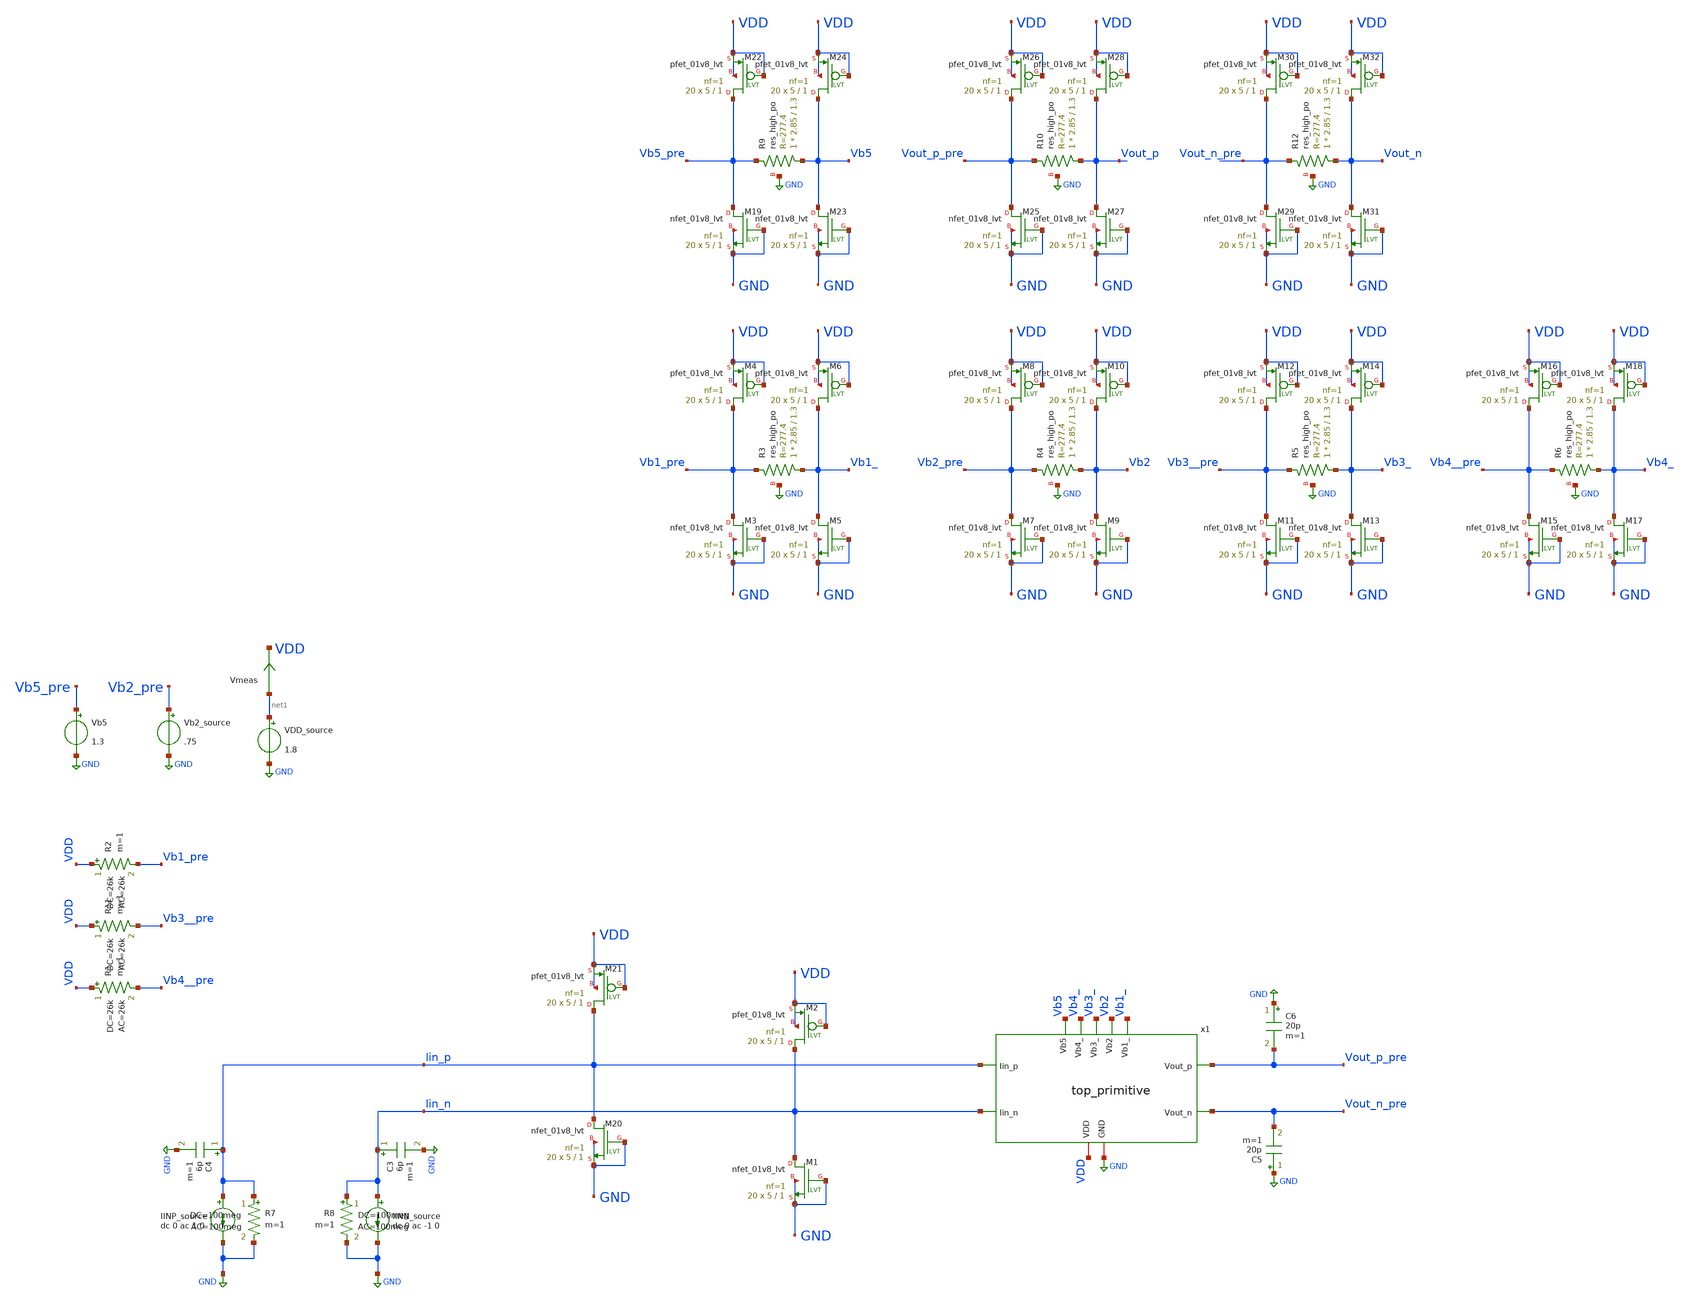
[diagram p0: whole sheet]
** sch_path: xschem/top_pex_tb.sch
**.subckt top_pex_tb
VDD_source net1 GND 1.8
Vmeas net1 VDD 0
.save i(vmeas)
Vb2_source Vb2_pre GND .75
C3 Iin_n GND 6p m=1
C4 Iin_p GND 6p m=1
IINP_source Iin_p GND dc 0 ac 1 0
IINN_source Iin_n GND dc 0 ac -1 0
C5 GND Vout_n_pre 20p m=1
C6 GND Vout_p_pre 20p m=1
R7 Iin_p GND 100meg ac=100meg m=1
R8 Iin_n GND 100meg ac=100meg m=1
Vb5 Vb5_pre GND 1.3
R2 VDD Vb1_pre 26k ac=26k m=1
R11 VDD Vb3__pre 26k ac=26k m=1
x1 Iin_p Iin_n Vb1_ Vb2 Vb3_ Vb4_ Vb5 VDD GND Vout_n_pre Vout_p_pre top_primitive
R1 VDD Vb4__pre 26k ac=26k m=1
XM20 Iin_p GND GND GND sky130_fd_pr__nfet_01v8_lvt L=1 W=5 nf=1 ad='int((nf+1)/2) * W/nf * 0.29' as='int((nf+2)/2) * W/nf * 0.29'
+ pd='2*int((nf+1)/2) * (W/nf + 0.29)' ps='2*int((nf+2)/2) * (W/nf + 0.29)' nrd='0.29 / W' nrs='0.29 / W'
+ sa=0 sb=0 sd=0 mult=20 m=20
XM21 Iin_p VDD VDD VDD sky130_fd_pr__pfet_01v8_lvt L=1 W=5 nf=1 ad='int((nf+1)/2) * W/nf * 0.29' as='int((nf+2)/2) * W/nf * 0.29'
+ pd='2*int((nf+1)/2) * (W/nf + 0.29)' ps='2*int((nf+2)/2) * (W/nf + 0.29)' nrd='0.29 / W' nrs='0.29 / W'
+ sa=0 sb=0 sd=0 mult=20 m=20
XM1 Iin_n GND GND GND sky130_fd_pr__nfet_01v8_lvt L=1 W=5 nf=1 ad='int((nf+1)/2) * W/nf * 0.29' as='int((nf+2)/2) * W/nf * 0.29'
+ pd='2*int((nf+1)/2) * (W/nf + 0.29)' ps='2*int((nf+2)/2) * (W/nf + 0.29)' nrd='0.29 / W' nrs='0.29 / W'
+ sa=0 sb=0 sd=0 mult=20 m=20
XM2 Iin_n VDD VDD VDD sky130_fd_pr__pfet_01v8_lvt L=1 W=5 nf=1 ad='int((nf+1)/2) * W/nf * 0.29' as='int((nf+2)/2) * W/nf * 0.29'
+ pd='2*int((nf+1)/2) * (W/nf + 0.29)' ps='2*int((nf+2)/2) * (W/nf + 0.29)' nrd='0.29 / W' nrs='0.29 / W'
+ sa=0 sb=0 sd=0 mult=20 m=20
XM3 Vb1_pre GND GND GND sky130_fd_pr__nfet_01v8_lvt L=1 W=5 nf=1 ad='int((nf+1)/2) * W/nf * 0.29' as='int((nf+2)/2) * W/nf * 0.29'
+ pd='2*int((nf+1)/2) * (W/nf + 0.29)' ps='2*int((nf+2)/2) * (W/nf + 0.29)' nrd='0.29 / W' nrs='0.29 / W'
+ sa=0 sb=0 sd=0 mult=20 m=20
XM4 Vb1_pre VDD VDD VDD sky130_fd_pr__pfet_01v8_lvt L=1 W=5 nf=1 ad='int((nf+1)/2) * W/nf * 0.29' as='int((nf+2)/2) * W/nf * 0.29'
+ pd='2*int((nf+1)/2) * (W/nf + 0.29)' ps='2*int((nf+2)/2) * (W/nf + 0.29)' nrd='0.29 / W' nrs='0.29 / W'
+ sa=0 sb=0 sd=0 mult=20 m=20
XM5 Vb1_ GND GND GND sky130_fd_pr__nfet_01v8_lvt L=1 W=5 nf=1 ad='int((nf+1)/2) * W/nf * 0.29' as='int((nf+2)/2) * W/nf * 0.29'
+ pd='2*int((nf+1)/2) * (W/nf + 0.29)' ps='2*int((nf+2)/2) * (W/nf + 0.29)' nrd='0.29 / W' nrs='0.29 / W'
+ sa=0 sb=0 sd=0 mult=20 m=20
XM6 Vb1_ VDD VDD VDD sky130_fd_pr__pfet_01v8_lvt L=1 W=5 nf=1 ad='int((nf+1)/2) * W/nf * 0.29' as='int((nf+2)/2) * W/nf * 0.29'
+ pd='2*int((nf+1)/2) * (W/nf + 0.29)' ps='2*int((nf+2)/2) * (W/nf + 0.29)' nrd='0.29 / W' nrs='0.29 / W'
+ sa=0 sb=0 sd=0 mult=20 m=20
XR3 Vb1_ Vb1_pre GND sky130_fd_pr__res_high_po W=2.85 L=1.3 mult=1 m=1
XM7 Vb2_pre GND GND GND sky130_fd_pr__nfet_01v8_lvt L=1 W=5 nf=1 ad='int((nf+1)/2) * W/nf * 0.29' as='int((nf+2)/2) * W/nf * 0.29'
+ pd='2*int((nf+1)/2) * (W/nf + 0.29)' ps='2*int((nf+2)/2) * (W/nf + 0.29)' nrd='0.29 / W' nrs='0.29 / W'
+ sa=0 sb=0 sd=0 mult=20 m=20
XM8 Vb2_pre VDD VDD VDD sky130_fd_pr__pfet_01v8_lvt L=1 W=5 nf=1 ad='int((nf+1)/2) * W/nf * 0.29' as='int((nf+2)/2) * W/nf * 0.29'
+ pd='2*int((nf+1)/2) * (W/nf + 0.29)' ps='2*int((nf+2)/2) * (W/nf + 0.29)' nrd='0.29 / W' nrs='0.29 / W'
+ sa=0 sb=0 sd=0 mult=20 m=20
XM9 Vb2 GND GND GND sky130_fd_pr__nfet_01v8_lvt L=1 W=5 nf=1 ad='int((nf+1)/2) * W/nf * 0.29' as='int((nf+2)/2) * W/nf * 0.29'
+ pd='2*int((nf+1)/2) * (W/nf + 0.29)' ps='2*int((nf+2)/2) * (W/nf + 0.29)' nrd='0.29 / W' nrs='0.29 / W'
+ sa=0 sb=0 sd=0 mult=20 m=20
XM10 Vb2 VDD VDD VDD sky130_fd_pr__pfet_01v8_lvt L=1 W=5 nf=1 ad='int((nf+1)/2) * W/nf * 0.29' as='int((nf+2)/2) * W/nf * 0.29'
+ pd='2*int((nf+1)/2) * (W/nf + 0.29)' ps='2*int((nf+2)/2) * (W/nf + 0.29)' nrd='0.29 / W' nrs='0.29 / W'
+ sa=0 sb=0 sd=0 mult=20 m=20
XR4 Vb2 Vb2_pre GND sky130_fd_pr__res_high_po W=2.85 L=1.3 mult=1 m=1
XM11 Vb3__pre GND GND GND sky130_fd_pr__nfet_01v8_lvt L=1 W=5 nf=1 ad='int((nf+1)/2) * W/nf * 0.29' as='int((nf+2)/2) * W/nf * 0.29'
+ pd='2*int((nf+1)/2) * (W/nf + 0.29)' ps='2*int((nf+2)/2) * (W/nf + 0.29)' nrd='0.29 / W' nrs='0.29 / W'
+ sa=0 sb=0 sd=0 mult=20 m=20
XM12 Vb3__pre VDD VDD VDD sky130_fd_pr__pfet_01v8_lvt L=1 W=5 nf=1 ad='int((nf+1)/2) * W/nf * 0.29' as='int((nf+2)/2) * W/nf * 0.29'
+ pd='2*int((nf+1)/2) * (W/nf + 0.29)' ps='2*int((nf+2)/2) * (W/nf + 0.29)' nrd='0.29 / W' nrs='0.29 / W'
+ sa=0 sb=0 sd=0 mult=20 m=20
XM13 Vb3_ GND GND GND sky130_fd_pr__nfet_01v8_lvt L=1 W=5 nf=1 ad='int((nf+1)/2) * W/nf * 0.29' as='int((nf+2)/2) * W/nf * 0.29'
+ pd='2*int((nf+1)/2) * (W/nf + 0.29)' ps='2*int((nf+2)/2) * (W/nf + 0.29)' nrd='0.29 / W' nrs='0.29 / W'
+ sa=0 sb=0 sd=0 mult=20 m=20
XM14 Vb3_ VDD VDD VDD sky130_fd_pr__pfet_01v8_lvt L=1 W=5 nf=1 ad='int((nf+1)/2) * W/nf * 0.29' as='int((nf+2)/2) * W/nf * 0.29'
+ pd='2*int((nf+1)/2) * (W/nf + 0.29)' ps='2*int((nf+2)/2) * (W/nf + 0.29)' nrd='0.29 / W' nrs='0.29 / W'
+ sa=0 sb=0 sd=0 mult=20 m=20
XR5 Vb3_ Vb3__pre GND sky130_fd_pr__res_high_po W=2.85 L=1.3 mult=1 m=1
XM15 Vb4__pre GND GND GND sky130_fd_pr__nfet_01v8_lvt L=1 W=5 nf=1 ad='int((nf+1)/2) * W/nf * 0.29' as='int((nf+2)/2) * W/nf * 0.29'
+ pd='2*int((nf+1)/2) * (W/nf + 0.29)' ps='2*int((nf+2)/2) * (W/nf + 0.29)' nrd='0.29 / W' nrs='0.29 / W'
+ sa=0 sb=0 sd=0 mult=20 m=20
XM16 Vb4__pre VDD VDD VDD sky130_fd_pr__pfet_01v8_lvt L=1 W=5 nf=1 ad='int((nf+1)/2) * W/nf * 0.29' as='int((nf+2)/2) * W/nf * 0.29'
+ pd='2*int((nf+1)/2) * (W/nf + 0.29)' ps='2*int((nf+2)/2) * (W/nf + 0.29)' nrd='0.29 / W' nrs='0.29 / W'
+ sa=0 sb=0 sd=0 mult=20 m=20
XM17 Vb4_ GND GND GND sky130_fd_pr__nfet_01v8_lvt L=1 W=5 nf=1 ad='int((nf+1)/2) * W/nf * 0.29' as='int((nf+2)/2) * W/nf * 0.29'
+ pd='2*int((nf+1)/2) * (W/nf + 0.29)' ps='2*int((nf+2)/2) * (W/nf + 0.29)' nrd='0.29 / W' nrs='0.29 / W'
+ sa=0 sb=0 sd=0 mult=20 m=20
XM18 Vb4_ VDD VDD VDD sky130_fd_pr__pfet_01v8_lvt L=1 W=5 nf=1 ad='int((nf+1)/2) * W/nf * 0.29' as='int((nf+2)/2) * W/nf * 0.29'
+ pd='2*int((nf+1)/2) * (W/nf + 0.29)' ps='2*int((nf+2)/2) * (W/nf + 0.29)' nrd='0.29 / W' nrs='0.29 / W'
+ sa=0 sb=0 sd=0 mult=20 m=20
XR6 Vb4_ Vb4__pre GND sky130_fd_pr__res_high_po W=2.85 L=1.3 mult=1 m=1
XM19 Vb5_pre GND GND GND sky130_fd_pr__nfet_01v8_lvt L=1 W=5 nf=1 ad='int((nf+1)/2) * W/nf * 0.29' as='int((nf+2)/2) * W/nf * 0.29'
+ pd='2*int((nf+1)/2) * (W/nf + 0.29)' ps='2*int((nf+2)/2) * (W/nf + 0.29)' nrd='0.29 / W' nrs='0.29 / W'
+ sa=0 sb=0 sd=0 mult=20 m=20
XM22 Vb5_pre VDD VDD VDD sky130_fd_pr__pfet_01v8_lvt L=1 W=5 nf=1 ad='int((nf+1)/2) * W/nf * 0.29' as='int((nf+2)/2) * W/nf * 0.29'
+ pd='2*int((nf+1)/2) * (W/nf + 0.29)' ps='2*int((nf+2)/2) * (W/nf + 0.29)' nrd='0.29 / W' nrs='0.29 / W'
+ sa=0 sb=0 sd=0 mult=20 m=20
XM23 Vb5 GND GND GND sky130_fd_pr__nfet_01v8_lvt L=1 W=5 nf=1 ad='int((nf+1)/2) * W/nf * 0.29' as='int((nf+2)/2) * W/nf * 0.29'
+ pd='2*int((nf+1)/2) * (W/nf + 0.29)' ps='2*int((nf+2)/2) * (W/nf + 0.29)' nrd='0.29 / W' nrs='0.29 / W'
+ sa=0 sb=0 sd=0 mult=20 m=20
XM24 Vb5 VDD VDD VDD sky130_fd_pr__pfet_01v8_lvt L=1 W=5 nf=1 ad='int((nf+1)/2) * W/nf * 0.29' as='int((nf+2)/2) * W/nf * 0.29'
+ pd='2*int((nf+1)/2) * (W/nf + 0.29)' ps='2*int((nf+2)/2) * (W/nf + 0.29)' nrd='0.29 / W' nrs='0.29 / W'
+ sa=0 sb=0 sd=0 mult=20 m=20
XR9 Vb5 Vb5_pre GND sky130_fd_pr__res_high_po W=2.85 L=1.3 mult=1 m=1
XM25 Vout_p_pre GND GND GND sky130_fd_pr__nfet_01v8_lvt L=1 W=5 nf=1 ad='int((nf+1)/2) * W/nf * 0.29'
+ as='int((nf+2)/2) * W/nf * 0.29' pd='2*int((nf+1)/2) * (W/nf + 0.29)' ps='2*int((nf+2)/2) * (W/nf + 0.29)'
+ nrd='0.29 / W' nrs='0.29 / W' sa=0 sb=0 sd=0 mult=20 m=20
XM26 Vout_p_pre VDD VDD VDD sky130_fd_pr__pfet_01v8_lvt L=1 W=5 nf=1 ad='int((nf+1)/2) * W/nf * 0.29'
+ as='int((nf+2)/2) * W/nf * 0.29' pd='2*int((nf+1)/2) * (W/nf + 0.29)' ps='2*int((nf+2)/2) * (W/nf + 0.29)'
+ nrd='0.29 / W' nrs='0.29 / W' sa=0 sb=0 sd=0 mult=20 m=20
XM27 Vout_p GND GND GND sky130_fd_pr__nfet_01v8_lvt L=1 W=5 nf=1 ad='int((nf+1)/2) * W/nf * 0.29' as='int((nf+2)/2) * W/nf * 0.29'
+ pd='2*int((nf+1)/2) * (W/nf + 0.29)' ps='2*int((nf+2)/2) * (W/nf + 0.29)' nrd='0.29 / W' nrs='0.29 / W'
+ sa=0 sb=0 sd=0 mult=20 m=20
XM28 Vout_p VDD VDD VDD sky130_fd_pr__pfet_01v8_lvt L=1 W=5 nf=1 ad='int((nf+1)/2) * W/nf * 0.29' as='int((nf+2)/2) * W/nf * 0.29'
+ pd='2*int((nf+1)/2) * (W/nf + 0.29)' ps='2*int((nf+2)/2) * (W/nf + 0.29)' nrd='0.29 / W' nrs='0.29 / W'
+ sa=0 sb=0 sd=0 mult=20 m=20
XR10 Vout_p Vout_p_pre GND sky130_fd_pr__res_high_po W=2.85 L=1.3 mult=1 m=1
XM29 Vout_n_pre GND GND GND sky130_fd_pr__nfet_01v8_lvt L=1 W=5 nf=1 ad='int((nf+1)/2) * W/nf * 0.29'
+ as='int((nf+2)/2) * W/nf * 0.29' pd='2*int((nf+1)/2) * (W/nf + 0.29)' ps='2*int((nf+2)/2) * (W/nf + 0.29)'
+ nrd='0.29 / W' nrs='0.29 / W' sa=0 sb=0 sd=0 mult=20 m=20
XM30 Vout_n_pre VDD VDD VDD sky130_fd_pr__pfet_01v8_lvt L=1 W=5 nf=1 ad='int((nf+1)/2) * W/nf * 0.29'
+ as='int((nf+2)/2) * W/nf * 0.29' pd='2*int((nf+1)/2) * (W/nf + 0.29)' ps='2*int((nf+2)/2) * (W/nf + 0.29)'
+ nrd='0.29 / W' nrs='0.29 / W' sa=0 sb=0 sd=0 mult=20 m=20
XM31 Vout_n GND GND GND sky130_fd_pr__nfet_01v8_lvt L=1 W=5 nf=1 ad='int((nf+1)/2) * W/nf * 0.29' as='int((nf+2)/2) * W/nf * 0.29'
+ pd='2*int((nf+1)/2) * (W/nf + 0.29)' ps='2*int((nf+2)/2) * (W/nf + 0.29)' nrd='0.29 / W' nrs='0.29 / W'
+ sa=0 sb=0 sd=0 mult=20 m=20
XM32 Vout_n VDD VDD VDD sky130_fd_pr__pfet_01v8_lvt L=1 W=5 nf=1 ad='int((nf+1)/2) * W/nf * 0.29' as='int((nf+2)/2) * W/nf * 0.29'
+ pd='2*int((nf+1)/2) * (W/nf + 0.29)' ps='2*int((nf+2)/2) * (W/nf + 0.29)' nrd='0.29 / W' nrs='0.29 / W'
+ sa=0 sb=0 sd=0 mult=20 m=20
XR12 Vout_n Vout_n_pre GND sky130_fd_pr__res_high_po W=2.85 L=1.3 mult=1 m=1
**** begin user architecture code

.include $::SKYWATER_MODELS/cells/nfet_01v8/sky130_fd_pr__nfet_01v8__tt.corner.spice
.include $::SKYWATER_MODELS/cells/pfet_01v8/sky130_fd_pr__pfet_01v8__tt.corner.spice
.include $::SKYWATER_MODELS/cells/nfet_01v8_lvt/sky130_fd_pr__nfet_01v8_lvt__tt.corner.spice
*.include $::SKYWATER_MODELS/cells/nfet_03v3_nvt/sky130_fd_pr__nfet_03v3_nvt__tt.corner.spice
*.include $::SKYWATER_MODELS/cells/nfet_05v0_nvt/sky130_fd_pr__nfet_05v0_nvt__tt.corner.spice
*.include $::SKYWATER_MODELS/cells/esd_nfet_01v8/sky130_fd_pr__esd_nfet_01v8__tt.corner.spice
.include $::SKYWATER_MODELS/cells/pfet_01v8_lvt/sky130_fd_pr__pfet_01v8_lvt__tt.corner.spice
*.include $::SKYWATER_MODELS/cells/pfet_01v8_hvt/sky130_fd_pr__pfet_01v8_hvt__tt.corner.spice
*.include $::SKYWATER_MODELS/models/corners/tt/nonfet.spice
* Mismatch parameters
.include $::SKYWATER_MODELS/cells/nfet_01v8/sky130_fd_pr__nfet_01v8__mismatch.corner.spice
.include $::SKYWATER_MODELS/cells/pfet_01v8/sky130_fd_pr__pfet_01v8__mismatch.corner.spice
.include $::SKYWATER_MODELS/cells/nfet_01v8_lvt/sky130_fd_pr__nfet_01v8_lvt__mismatch.corner.spice
.include $::SKYWATER_MODELS/cells/pfet_01v8_lvt/sky130_fd_pr__pfet_01v8_lvt__mismatch.corner.spice
*.include $::SKYWATER_MODELS/cells/pfet_01v8_hvt/sky130_fd_pr__pfet_01v8_hvt__mismatch.corner.spice
*.include $::SKYWATER_MODELS/cells/nfet_g5v0d10v5/sky130_fd_pr__nfet_g5v0d10v5__mismatch.corner.spice
*.include $::SKYWATER_MODELS/cells/pfet_g5v0d10v5/sky130_fd_pr__pfet_g5v0d10v5__mismatch.corner.spice
*.include $::SKYWATER_MODELS/cells/nfet_05v0_nvt/sky130_fd_pr__nfet_05v0_nvt__mismatch.corner.spice
*.include $::SKYWATER_MODELS/cells/nfet_03v3_nvt/sky130_fd_pr__nfet_03v3_nvt__mismatch.corner.spice
* Resistor$::SKYWATER_MODELS/Capacitor
.include $::SKYWATER_MODELS/models/r+c/res_typical__cap_typical.spice
.include $::SKYWATER_MODELS/models/r+c/res_typical__cap_typical__lin.spice
* Special cells
*.include $::SKYWATER_MODELS/models/corners/tt/specialized_cells.spice
* All models
.include $::SKYWATER_MODELS/models/all.spice
* Corner
*.include $::SKYWATER_MODELS/models/corners/tt/rf.spice
.include /home/jared/Documents/GS_Design/sscs_pico_chip_4/pex/top_pex.spice


.option savecurrents
.control
save all
*NFET

save @m.xm90.msky130_fd_pr__nfet_01v8[vds] @m.xm90.msky130_fd_pr__nfet_01v8[gm]
+ @m.xm90.msky130_fd_pr__nfet_01v8[vth] @m.xm90.msky130_fd_pr__nfet_01v8[vgs] @m.xm90.msky130_fd_pr__nfet_01v8[id]
+ @m.xm90.msky130_fd_pr__nfet_01v8[gds] @m.xm90.msky130_fd_pr__nfet_01v8[cgg] @m.xm90.msky130_fd_pr__nfet_01v8[cgs]
+ @m.xm90.msky130_fd_pr__nfet_01v8[cgd] @m.xm90.msky130_fd_pr__nfet_01v8[cgb] @m.xm90.msky130_fd_pr__nfet_01v8[cdg]
+ @m.xm90.msky130_fd_pr__nfet_01v8[cds] @m.xm90.msky130_fd_pr__nfet_01v8[cdd] @m.xm90.msky130_fd_pr__nfet_01v8[cdb]
+ @m.xm90.msky130_fd_pr__nfet_01v8[csg] @m.xm90.msky130_fd_pr__nfet_01v8[css] @m.xm90.msky130_fd_pr__nfet_01v8[csd]
+ @m.xm90.msky130_fd_pr__nfet_01v8[csb] @m.xm90.msky130_fd_pr__nfet_01v8[cbg] @m.xm90.msky130_fd_pr__nfet_01v8[cbs]
+ @m.xm90.msky130_fd_pr__nfet_01v8[cbd] @m.xm90.msky130_fd_pr__nfet_01v8[cbb]
save @m.xm1.msky130_fd_pr__nfet_01v8[vds] @m.xm1.msky130_fd_pr__nfet_01v8[gm]
+ @m.xm1.msky130_fd_pr__nfet_01v8[vth] @m.xm1.msky130_fd_pr__nfet_01v8[vgs] @m.xm1.msky130_fd_pr__nfet_01v8[id]
+ @m.xm1.msky130_fd_pr__nfet_01v8[gds] @m.xm1.msky130_fd_pr__nfet_01v8[cgg] @m.xm1.msky130_fd_pr__nfet_01v8[cgs]
+ @m.xm1.msky130_fd_pr__nfet_01v8[cgd] @m.xm1.msky130_fd_pr__nfet_01v8[cgb] @m.xm1.msky130_fd_pr__nfet_01v8[cdg]
+ @m.xm1.msky130_fd_pr__nfet_01v8[cds] @m.xm1.msky130_fd_pr__nfet_01v8[cdd] @m.xm1.msky130_fd_pr__nfet_01v8[cdb]
+ @m.xm1.msky130_fd_pr__nfet_01v8[csg] @m.xm1.msky130_fd_pr__nfet_01v8[css] @m.xm1.msky130_fd_pr__nfet_01v8[csd]
+ @m.xm1.msky130_fd_pr__nfet_01v8[csb] @m.xm1.msky130_fd_pr__nfet_01v8[cbg] @m.xm1.msky130_fd_pr__nfet_01v8[cbs]
+ @m.xm1.msky130_fd_pr__nfet_01v8[cbd] @m.xm1.msky130_fd_pr__nfet_01v8[cbb]
save @m.xm2.msky130_fd_pr__nfet_01v8[vds] @m.xm2.msky130_fd_pr__nfet_01v8[gm]
+ @m.xm2.msky130_fd_pr__nfet_01v8[vth] @m.xm2.msky130_fd_pr__nfet_01v8[vgs] @m.xm2.msky130_fd_pr__nfet_01v8[id]
+ @m.xm2.msky130_fd_pr__nfet_01v8[gds] @m.xm2.msky130_fd_pr__nfet_01v8[cgg] @m.xm2.msky130_fd_pr__nfet_01v8[cgs]
+ @m.xm2.msky130_fd_pr__nfet_01v8[cgd] @m.xm2.msky130_fd_pr__nfet_01v8[cgb] @m.xm2.msky130_fd_pr__nfet_01v8[cdg]
+ @m.xm2.msky130_fd_pr__nfet_01v8[cds] @m.xm2.msky130_fd_pr__nfet_01v8[cdd] @m.xm2.msky130_fd_pr__nfet_01v8[cdb]
+ @m.xm2.msky130_fd_pr__nfet_01v8[csg] @m.xm2.msky130_fd_pr__nfet_01v8[css] @m.xm2.msky130_fd_pr__nfet_01v8[csd]
+ @m.xm2.msky130_fd_pr__nfet_01v8[csb] @m.xm2.msky130_fd_pr__nfet_01v8[cbg] @m.xm2.msky130_fd_pr__nfet_01v8[cbs]
+ @m.xm2.msky130_fd_pr__nfet_01v8[cbd] @m.xm2.msky130_fd_pr__nfet_01v8[cbb]
save @m.xm3.msky130_fd_pr__nfet_01v8[vds] @m.xm3.msky130_fd_pr__nfet_01v8[gm]
+ @m.xm3.msky130_fd_pr__nfet_01v8[vth] @m.xm3.msky130_fd_pr__nfet_01v8[vgs] @m.xm3.msky130_fd_pr__nfet_01v8[id]
+ @m.xm3.msky130_fd_pr__nfet_01v8[gds] @m.xm3.msky130_fd_pr__nfet_01v8[cgg] @m.xm3.msky130_fd_pr__nfet_01v8[cgs]
+ @m.xm3.msky130_fd_pr__nfet_01v8[cgd] @m.xm3.msky130_fd_pr__nfet_01v8[cgb] @m.xm3.msky130_fd_pr__nfet_01v8[cdg]
+ @m.xm3.msky130_fd_pr__nfet_01v8[cds] @m.xm3.msky130_fd_pr__nfet_01v8[cdd] @m.xm3.msky130_fd_pr__nfet_01v8[cdb]
+ @m.xm3.msky130_fd_pr__nfet_01v8[csg] @m.xm3.msky130_fd_pr__nfet_01v8[css] @m.xm3.msky130_fd_pr__nfet_01v8[csd]
+ @m.xm3.msky130_fd_pr__nfet_01v8[csb] @m.xm3.msky130_fd_pr__nfet_01v8[cbg] @m.xm3.msky130_fd_pr__nfet_01v8[cbs]
+ @m.xm3.msky130_fd_pr__nfet_01v8[cbd] @m.xm3.msky130_fd_pr__nfet_01v8[cbb]
save @m.xm6.msky130_fd_pr__nfet_01v8[vds] @m.xm6.msky130_fd_pr__nfet_01v8[gm]
+ @m.xm6.msky130_fd_pr__nfet_01v8[vth] @m.xm6.msky130_fd_pr__nfet_01v8[vgs] @m.xm6.msky130_fd_pr__nfet_01v8[id]
+ @m.xm6.msky130_fd_pr__nfet_01v8[gds] @m.xm6.msky130_fd_pr__nfet_01v8[cgg] @m.xm6.msky130_fd_pr__nfet_01v8[cgs]
+ @m.xm6.msky130_fd_pr__nfet_01v8[cgd] @m.xm6.msky130_fd_pr__nfet_01v8[cgb] @m.xm6.msky130_fd_pr__nfet_01v8[cdg]
+ @m.xm6.msky130_fd_pr__nfet_01v8[cds] @m.xm6.msky130_fd_pr__nfet_01v8[cdd] @m.xm6.msky130_fd_pr__nfet_01v8[cdb]
+ @m.xm6.msky130_fd_pr__nfet_01v8[csg] @m.xm6.msky130_fd_pr__nfet_01v8[css] @m.xm6.msky130_fd_pr__nfet_01v8[csd]
+ @m.xm6.msky130_fd_pr__nfet_01v8[csb] @m.xm6.msky130_fd_pr__nfet_01v8[cbg] @m.xm6.msky130_fd_pr__nfet_01v8[cbs]
+ @m.xm6.msky130_fd_pr__nfet_01v8[cbd] @m.xm6.msky130_fd_pr__nfet_01v8[cbb]
save @m.xm7.msky130_fd_pr__nfet_01v8[vds] @m.xm7.msky130_fd_pr__nfet_01v8[gm]
+ @m.xm7.msky130_fd_pr__nfet_01v8[vth] @m.xm7.msky130_fd_pr__nfet_01v8[vgs] @m.xm7.msky130_fd_pr__nfet_01v8[id]
+ @m.xm7.msky130_fd_pr__nfet_01v8[gds] @m.xm7.msky130_fd_pr__nfet_01v8[cgg] @m.xm7.msky130_fd_pr__nfet_01v8[cgs]
+ @m.xm7.msky130_fd_pr__nfet_01v8[cgd] @m.xm7.msky130_fd_pr__nfet_01v8[cgb] @m.xm7.msky130_fd_pr__nfet_01v8[cdg]
+ @m.xm7.msky130_fd_pr__nfet_01v8[cds] @m.xm7.msky130_fd_pr__nfet_01v8[cdd] @m.xm7.msky130_fd_pr__nfet_01v8[cdb]
+ @m.xm7.msky130_fd_pr__nfet_01v8[csg] @m.xm7.msky130_fd_pr__nfet_01v8[css] @m.xm7.msky130_fd_pr__nfet_01v8[csd]
+ @m.xm7.msky130_fd_pr__nfet_01v8[csb] @m.xm7.msky130_fd_pr__nfet_01v8[cbg] @m.xm7.msky130_fd_pr__nfet_01v8[cbs]
+ @m.xm7.msky130_fd_pr__nfet_01v8[cbd] @m.xm7.msky130_fd_pr__nfet_01v8[cbb]
save @m.xm8.msky130_fd_pr__nfet_01v8[vds] @m.xm8.msky130_fd_pr__nfet_01v8[gm]
+ @m.xm8.msky130_fd_pr__nfet_01v8[vth] @m.xm8.msky130_fd_pr__nfet_01v8[vgs] @m.xm8.msky130_fd_pr__nfet_01v8[id]
+ @m.xm8.msky130_fd_pr__nfet_01v8[gds] @m.xm8.msky130_fd_pr__nfet_01v8[cgg] @m.xm8.msky130_fd_pr__nfet_01v8[cgs]
+ @m.xm8.msky130_fd_pr__nfet_01v8[cgd] @m.xm8.msky130_fd_pr__nfet_01v8[cgb] @m.xm8.msky130_fd_pr__nfet_01v8[cdg]
+ @m.xm8.msky130_fd_pr__nfet_01v8[cds] @m.xm8.msky130_fd_pr__nfet_01v8[cdd] @m.xm8.msky130_fd_pr__nfet_01v8[cdb]
+ @m.xm8.msky130_fd_pr__nfet_01v8[csg] @m.xm8.msky130_fd_pr__nfet_01v8[css] @m.xm8.msky130_fd_pr__nfet_01v8[csd]
+ @m.xm8.msky130_fd_pr__nfet_01v8[csb] @m.xm8.msky130_fd_pr__nfet_01v8[cbg] @m.xm8.msky130_fd_pr__nfet_01v8[cbs]
+ @m.xm8.msky130_fd_pr__nfet_01v8[cbd] @m.xm8.msky130_fd_pr__nfet_01v8[cbb]
save @m.xm11.msky130_fd_pr__nfet_01v8[vds] @m.xm11.msky130_fd_pr__nfet_01v8[gm]
+ @m.xm11.msky130_fd_pr__nfet_01v8[vth] @m.xm11.msky130_fd_pr__nfet_01v8[vgs] @m.xm11.msky130_fd_pr__nfet_01v8[id]
+ @m.xm11.msky130_fd_pr__nfet_01v8[gds] @m.xm11.msky130_fd_pr__nfet_01v8[cgg] @m.xm11.msky130_fd_pr__nfet_01v8[cgs]
+ @m.xm11.msky130_fd_pr__nfet_01v8[cgd] @m.xm11.msky130_fd_pr__nfet_01v8[cgb] @m.xm11.msky130_fd_pr__nfet_01v8[cdg]
+ @m.xm11.msky130_fd_pr__nfet_01v8[cds] @m.xm11.msky130_fd_pr__nfet_01v8[cdd] @m.xm11.msky130_fd_pr__nfet_01v8[cdb]
+ @m.xm11.msky130_fd_pr__nfet_01v8[csg] @m.xm11.msky130_fd_pr__nfet_01v8[css] @m.xm11.msky130_fd_pr__nfet_01v8[csd]
+ @m.xm11.msky130_fd_pr__nfet_01v8[csb] @m.xm11.msky130_fd_pr__nfet_01v8[cbg] @m.xm11.msky130_fd_pr__nfet_01v8[cbs]
+ @m.xm11.msky130_fd_pr__nfet_01v8[cbd] @m.xm11.msky130_fd_pr__nfet_01v8[cbb]
save @m.xm12.msky130_fd_pr__nfet_01v8[vds] @m.xm12.msky130_fd_pr__nfet_01v8[gm]
+ @m.xm12.msky130_fd_pr__nfet_01v8[vth] @m.xm12.msky130_fd_pr__nfet_01v8[vgs] @m.xm12.msky130_fd_pr__nfet_01v8[id]
+ @m.xm12.msky130_fd_pr__nfet_01v8[gds] @m.xm12.msky130_fd_pr__nfet_01v8[cgg] @m.xm12.msky130_fd_pr__nfet_01v8[cgs]
+ @m.xm12.msky130_fd_pr__nfet_01v8[cgd] @m.xm12.msky130_fd_pr__nfet_01v8[cgb] @m.xm12.msky130_fd_pr__nfet_01v8[cdg]
+ @m.xm12.msky130_fd_pr__nfet_01v8[cds] @m.xm12.msky130_fd_pr__nfet_01v8[cdd] @m.xm12.msky130_fd_pr__nfet_01v8[cdb]
+ @m.xm12.msky130_fd_pr__nfet_01v8[csg] @m.xm12.msky130_fd_pr__nfet_01v8[css] @m.xm12.msky130_fd_pr__nfet_01v8[csd]
+ @m.xm12.msky130_fd_pr__nfet_01v8[csb] @m.xm12.msky130_fd_pr__nfet_01v8[cbg] @m.xm12.msky130_fd_pr__nfet_01v8[cbs]
+ @m.xm12.msky130_fd_pr__nfet_01v8[cbd] @m.xm12.msky130_fd_pr__nfet_01v8[cbb]
save @m.xm16.msky130_fd_pr__nfet_01v8[vds] @m.xm16.msky130_fd_pr__nfet_01v8[gm]
+ @m.xm16.msky130_fd_pr__nfet_01v8[vth] @m.xm16.msky130_fd_pr__nfet_01v8[vgs] @m.xm16.msky130_fd_pr__nfet_01v8[id]
+ @m.xm16.msky130_fd_pr__nfet_01v8[gds] @m.xm16.msky130_fd_pr__nfet_01v8[cgg] @m.xm16.msky130_fd_pr__nfet_01v8[cgs]
+ @m.xm16.msky130_fd_pr__nfet_01v8[cgd] @m.xm16.msky130_fd_pr__nfet_01v8[cgb] @m.xm16.msky130_fd_pr__nfet_01v8[cdg]
+ @m.xm16.msky130_fd_pr__nfet_01v8[cds] @m.xm16.msky130_fd_pr__nfet_01v8[cdd] @m.xm16.msky130_fd_pr__nfet_01v8[cdb]
+ @m.xm16.msky130_fd_pr__nfet_01v8[csg] @m.xm16.msky130_fd_pr__nfet_01v8[css] @m.xm16.msky130_fd_pr__nfet_01v8[csd]
+ @m.xm16.msky130_fd_pr__nfet_01v8[csb] @m.xm16.msky130_fd_pr__nfet_01v8[cbg] @m.xm16.msky130_fd_pr__nfet_01v8[cbs]
+ @m.xm16.msky130_fd_pr__nfet_01v8[cbd] @m.xm16.msky130_fd_pr__nfet_01v8[cbb]
save @m.xm17.msky130_fd_pr__nfet_01v8_lvt[vds] @m.xm17.msky130_fd_pr__nfet_01v8_lvt[gm]
+ @m.xm17.msky130_fd_pr__nfet_01v8_lvt[vth] @m.xm17.msky130_fd_pr__nfet_01v8_lvt[vgs] @m.xm17.msky130_fd_pr__nfet_01v8_lvt[id]
+ @m.xm17.msky130_fd_pr__nfet_01v8_lvt[gds] @m.xm17.msky130_fd_pr__nfet_01v8_lvt[cgg] @m.xm17.msky130_fd_pr__nfet_01v8_lvt[cgs]
+ @m.xm17.msky130_fd_pr__nfet_01v8_lvt[cgd] @m.xm17.msky130_fd_pr__nfet_01v8_lvt[cgb] @m.xm17.msky130_fd_pr__nfet_01v8_lvt[cdg]
+ @m.xm17.msky130_fd_pr__nfet_01v8_lvt[cds] @m.xm17.msky130_fd_pr__nfet_01v8_lvt[cdd] @m.xm17.msky130_fd_pr__nfet_01v8_lvt[cdb]
+ @m.xm17.msky130_fd_pr__nfet_01v8_lvt[csg] @m.xm17.msky130_fd_pr__nfet_01v8_lvt[css] @m.xm17.msky130_fd_pr__nfet_01v8_lvt[csd]
+ @m.xm17.msky130_fd_pr__nfet_01v8_lvt[csb] @m.xm17.msky130_fd_pr__nfet_01v8_lvt[cbg] @m.xm17.msky130_fd_pr__nfet_01v8_lvt[cbs]
+ @m.xm17.msky130_fd_pr__nfet_01v8_lvt[cbd] @m.xm17.msky130_fd_pr__nfet_01v8_lvt[cbb]
save @m.xm18.msky130_fd_pr__nfet_01v8_lvt[vds] @m.xm18.msky130_fd_pr__nfet_01v8_lvt[gm]
+ @m.xm18.msky130_fd_pr__nfet_01v8_lvt[vth] @m.xm18.msky130_fd_pr__nfet_01v8_lvt[vgs] @m.xm18.msky130_fd_pr__nfet_01v8_lvt[id]
+ @m.xm18.msky130_fd_pr__nfet_01v8_lvt[gds] @m.xm18.msky130_fd_pr__nfet_01v8_lvt[cgg] @m.xm18.msky130_fd_pr__nfet_01v8_lvt[cgs]
+ @m.xm18.msky130_fd_pr__nfet_01v8_lvt[cgd] @m.xm18.msky130_fd_pr__nfet_01v8_lvt[cgb] @m.xm18.msky130_fd_pr__nfet_01v8_lvt[cdg]
+ @m.xm18.msky130_fd_pr__nfet_01v8_lvt[cds] @m.xm18.msky130_fd_pr__nfet_01v8_lvt[cdd] @m.xm18.msky130_fd_pr__nfet_01v8_lvt[cdb]
+ @m.xm18.msky130_fd_pr__nfet_01v8_lvt[csg] @m.xm18.msky130_fd_pr__nfet_01v8_lvt[css] @m.xm18.msky130_fd_pr__nfet_01v8_lvt[csd]
+ @m.xm18.msky130_fd_pr__nfet_01v8_lvt[csb] @m.xm18.msky130_fd_pr__nfet_01v8_lvt[cbg] @m.xm18.msky130_fd_pr__nfet_01v8_lvt[cbs]
+ @m.xm18.msky130_fd_pr__nfet_01v8_lvt[cbd] @m.xm18.msky130_fd_pr__nfet_01v8_lvt[cbb]
save @m.xm19.msky130_fd_pr__nfet_01v8[vds] @m.xm19.msky130_fd_pr__nfet_01v8[gm]
+ @m.xm19.msky130_fd_pr__nfet_01v8[vth] @m.xm19.msky130_fd_pr__nfet_01v8[vgs] @m.xm19.msky130_fd_pr__nfet_01v8[id]
+ @m.xm19.msky130_fd_pr__nfet_01v8[gds] @m.xm19.msky130_fd_pr__nfet_01v8[cgg] @m.xm19.msky130_fd_pr__nfet_01v8[cgs]
+ @m.xm19.msky130_fd_pr__nfet_01v8[cgd] @m.xm19.msky130_fd_pr__nfet_01v8[cgb] @m.xm19.msky130_fd_pr__nfet_01v8[cdg]
+ @m.xm19.msky130_fd_pr__nfet_01v8[cds] @m.xm19.msky130_fd_pr__nfet_01v8[cdd] @m.xm19.msky130_fd_pr__nfet_01v8[cdb]
+ @m.xm19.msky130_fd_pr__nfet_01v8[csg] @m.xm19.msky130_fd_pr__nfet_01v8[css] @m.xm19.msky130_fd_pr__nfet_01v8[csd]
+ @m.xm19.msky130_fd_pr__nfet_01v8[csb] @m.xm19.msky130_fd_pr__nfet_01v8[cbg] @m.xm19.msky130_fd_pr__nfet_01v8[cbs]
+ @m.xm19.msky130_fd_pr__nfet_01v8[cbd] @m.xm19.msky130_fd_pr__nfet_01v8[cbb]
save @m.xm30.msky130_fd_pr__nfet_01v8[vds] @m.xm30.msky130_fd_pr__nfet_01v8[gm]
+ @m.xm30.msky130_fd_pr__nfet_01v8[vth] @m.xm30.msky130_fd_pr__nfet_01v8[vgs] @m.xm30.msky130_fd_pr__nfet_01v8[id]
+ @m.xm30.msky130_fd_pr__nfet_01v8[gds] @m.xm30.msky130_fd_pr__nfet_01v8[cgg] @m.xm30.msky130_fd_pr__nfet_01v8[cgs]
+ @m.xm30.msky130_fd_pr__nfet_01v8[cgd] @m.xm30.msky130_fd_pr__nfet_01v8[cgb] @m.xm30.msky130_fd_pr__nfet_01v8[cdg]
+ @m.xm30.msky130_fd_pr__nfet_01v8[cds] @m.xm30.msky130_fd_pr__nfet_01v8[cdd] @m.xm30.msky130_fd_pr__nfet_01v8[cdb]
+ @m.xm30.msky130_fd_pr__nfet_01v8[csg] @m.xm30.msky130_fd_pr__nfet_01v8[css] @m.xm30.msky130_fd_pr__nfet_01v8[csd]
+ @m.xm30.msky130_fd_pr__nfet_01v8[csb] @m.xm30.msky130_fd_pr__nfet_01v8[cbg] @m.xm30.msky130_fd_pr__nfet_01v8[cbs]
+ @m.xm30.msky130_fd_pr__nfet_01v8[cbd] @m.xm30.msky130_fd_pr__nfet_01v8[cbb]
save @m.xm26.msky130_fd_pr__nfet_01v8[vds] @m.xm26.msky130_fd_pr__nfet_01v8[gm]
+ @m.xm26.msky130_fd_pr__nfet_01v8[vth] @m.xm26.msky130_fd_pr__nfet_01v8[vgs] @m.xm26.msky130_fd_pr__nfet_01v8[id]
+ @m.xm26.msky130_fd_pr__nfet_01v8[gds] @m.xm26.msky130_fd_pr__nfet_01v8[cgg] @m.xm26.msky130_fd_pr__nfet_01v8[cgs]
+ @m.xm26.msky130_fd_pr__nfet_01v8[cgd] @m.xm26.msky130_fd_pr__nfet_01v8[cgb] @m.xm26.msky130_fd_pr__nfet_01v8[cdg]
+ @m.xm26.msky130_fd_pr__nfet_01v8[cds] @m.xm26.msky130_fd_pr__nfet_01v8[cdd] @m.xm26.msky130_fd_pr__nfet_01v8[cdb]
+ @m.xm26.msky130_fd_pr__nfet_01v8[csg] @m.xm26.msky130_fd_pr__nfet_01v8[css] @m.xm26.msky130_fd_pr__nfet_01v8[csd]
+ @m.xm26.msky130_fd_pr__nfet_01v8[csb] @m.xm26.msky130_fd_pr__nfet_01v8[cbg] @m.xm26.msky130_fd_pr__nfet_01v8[cbs]
+ @m.xm26.msky130_fd_pr__nfet_01v8[cbd] @m.xm26.msky130_fd_pr__nfet_01v8[cbb]
save @m.xm27.msky130_fd_pr__nfet_01v8[vds] @m.xm27.msky130_fd_pr__nfet_01v8[gm]
+ @m.xm27.msky130_fd_pr__nfet_01v8[vth] @m.xm27.msky130_fd_pr__nfet_01v8[vgs] @m.xm27.msky130_fd_pr__nfet_01v8[id]
+ @m.xm27.msky130_fd_pr__nfet_01v8[gds] @m.xm27.msky130_fd_pr__nfet_01v8[cgg] @m.xm27.msky130_fd_pr__nfet_01v8[cgs]
+ @m.xm27.msky130_fd_pr__nfet_01v8[cgd] @m.xm27.msky130_fd_pr__nfet_01v8[cgb] @m.xm27.msky130_fd_pr__nfet_01v8[cdg]
+ @m.xm27.msky130_fd_pr__nfet_01v8[cds] @m.xm27.msky130_fd_pr__nfet_01v8[cdd] @m.xm27.msky130_fd_pr__nfet_01v8[cdb]
+ @m.xm27.msky130_fd_pr__nfet_01v8[csg] @m.xm27.msky130_fd_pr__nfet_01v8[css] @m.xm27.msky130_fd_pr__nfet_01v8[csd]
+ @m.xm27.msky130_fd_pr__nfet_01v8[csb] @m.xm27.msky130_fd_pr__nfet_01v8[cbg] @m.xm27.msky130_fd_pr__nfet_01v8[cbs]
+ @m.xm27.msky130_fd_pr__nfet_01v8[cbd] @m.xm27.msky130_fd_pr__nfet_01v8[cbb]

*PFET

save @m.xm91.msky130_fd_pr__pfet_01v8[vds] @m.xm91.msky130_fd_pr__pfet_01v8[gm]
+ @m.xm91.msky130_fd_pr__pfet_01v8[vth] @m.xm91.msky130_fd_pr__pfet_01v8[vgs] @m.xm91.msky130_fd_pr__pfet_01v8[id]
+ @m.xm91.msky130_fd_pr__pfet_01v8[gds] @m.xm91.msky130_fd_pr__pfet_01v8[cgg] @m.xm91.msky130_fd_pr__pfet_01v8[cgs]
+ @m.xm91.msky130_fd_pr__pfet_01v8[cgd] @m.xm91.msky130_fd_pr__pfet_01v8[cgb] @m.xm91.msky130_fd_pr__pfet_01v8[cdg]
+ @m.xm91.msky130_fd_pr__pfet_01v8[cds] @m.xm91.msky130_fd_pr__pfet_01v8[cdd] @m.xm91.msky130_fd_pr__pfet_01v8[cdb]
+ @m.xm91.msky130_fd_pr__pfet_01v8[csg] @m.xm91.msky130_fd_pr__pfet_01v8[css] @m.xm91.msky130_fd_pr__pfet_01v8[csd]
+ @m.xm91.msky130_fd_pr__pfet_01v8[csb] @m.xm91.msky130_fd_pr__pfet_01v8[cbg] @m.xm91.msky130_fd_pr__pfet_01v8[cbs]
+ @m.xm91.msky130_fd_pr__pfet_01v8[cbd] @m.xm91.msky130_fd_pr__pfet_01v8[cbb]
save @m.xm4.msky130_fd_pr__pfet_01v8[vds] @m.xm4.msky130_fd_pr__pfet_01v8[gm]
+ @m.xm4.msky130_fd_pr__pfet_01v8[vth] @m.xm4.msky130_fd_pr__pfet_01v8[vgs] @m.xm4.msky130_fd_pr__pfet_01v8[id]
+ @m.xm4.msky130_fd_pr__pfet_01v8[gds] @m.xm4.msky130_fd_pr__pfet_01v8[cgg] @m.xm4.msky130_fd_pr__pfet_01v8[cgs]
+ @m.xm4.msky130_fd_pr__pfet_01v8[cgd] @m.xm4.msky130_fd_pr__pfet_01v8[cgb] @m.xm4.msky130_fd_pr__pfet_01v8[cdg]
+ @m.xm4.msky130_fd_pr__pfet_01v8[cds] @m.xm4.msky130_fd_pr__pfet_01v8[cdd] @m.xm4.msky130_fd_pr__pfet_01v8[cdb]
+ @m.xm4.msky130_fd_pr__pfet_01v8[csg] @m.xm4.msky130_fd_pr__pfet_01v8[css] @m.xm4.msky130_fd_pr__pfet_01v8[csd]
+ @m.xm4.msky130_fd_pr__pfet_01v8[csb] @m.xm4.msky130_fd_pr__pfet_01v8[cbg] @m.xm4.msky130_fd_pr__pfet_01v8[cbs]
+ @m.xm4.msky130_fd_pr__pfet_01v8[cbd] @m.xm4.msky130_fd_pr__pfet_01v8[cbb]
save @m.xm5.msky130_fd_pr__pfet_01v8[vds] @m.xm5.msky130_fd_pr__pfet_01v8[gm]
+ @m.xm5.msky130_fd_pr__pfet_01v8[vth] @m.xm5.msky130_fd_pr__pfet_01v8[vgs] @m.xm5.msky130_fd_pr__pfet_01v8[id]
+ @m.xm5.msky130_fd_pr__pfet_01v8[gds] @m.xm5.msky130_fd_pr__pfet_01v8[cgg] @m.xm5.msky130_fd_pr__pfet_01v8[cgs]
+ @m.xm5.msky130_fd_pr__pfet_01v8[cgd] @m.xm5.msky130_fd_pr__pfet_01v8[cgb] @m.xm5.msky130_fd_pr__pfet_01v8[cdg]
+ @m.xm5.msky130_fd_pr__pfet_01v8[cds] @m.xm5.msky130_fd_pr__pfet_01v8[cdd] @m.xm5.msky130_fd_pr__pfet_01v8[cdb]
+ @m.xm5.msky130_fd_pr__pfet_01v8[csg] @m.xm5.msky130_fd_pr__pfet_01v8[css] @m.xm5.msky130_fd_pr__pfet_01v8[csd]
+ @m.xm5.msky130_fd_pr__pfet_01v8[csb] @m.xm5.msky130_fd_pr__pfet_01v8[cbg] @m.xm5.msky130_fd_pr__pfet_01v8[cbs]
+ @m.xm5.msky130_fd_pr__pfet_01v8[cbd] @m.xm5.msky130_fd_pr__pfet_01v8[cbb]
save @m.xm9.msky130_fd_pr__pfet_01v8[vds] @m.xm9.msky130_fd_pr__pfet_01v8[gm]
+ @m.xm9.msky130_fd_pr__pfet_01v8[vth] @m.xm9.msky130_fd_pr__pfet_01v8[vgs] @m.xm9.msky130_fd_pr__pfet_01v8[id]
+ @m.xm9.msky130_fd_pr__pfet_01v8[gds] @m.xm9.msky130_fd_pr__pfet_01v8[cgg] @m.xm9.msky130_fd_pr__pfet_01v8[cgs]
+ @m.xm9.msky130_fd_pr__pfet_01v8[cgd] @m.xm9.msky130_fd_pr__pfet_01v8[cgb] @m.xm9.msky130_fd_pr__pfet_01v8[cdg]
+ @m.xm9.msky130_fd_pr__pfet_01v8[cds] @m.xm9.msky130_fd_pr__pfet_01v8[cdd] @m.xm9.msky130_fd_pr__pfet_01v8[cdb]
+ @m.xm9.msky130_fd_pr__pfet_01v8[csg] @m.xm9.msky130_fd_pr__pfet_01v8[css] @m.xm9.msky130_fd_pr__pfet_01v8[csd]
+ @m.xm9.msky130_fd_pr__pfet_01v8[csb] @m.xm9.msky130_fd_pr__pfet_01v8[cbg] @m.xm9.msky130_fd_pr__pfet_01v8[cbs]
+ @m.xm9.msky130_fd_pr__pfet_01v8[cbd] @m.xm9.msky130_fd_pr__pfet_01v8[cbb]
save @m.xm10.msky130_fd_pr__pfet_01v8[vds] @m.xm10.msky130_fd_pr__pfet_01v8[gm]
+ @m.xm10.msky130_fd_pr__pfet_01v8[vth] @m.xm10.msky130_fd_pr__pfet_01v8[vgs] @m.xm10.msky130_fd_pr__pfet_01v8[id]
+ @m.xm10.msky130_fd_pr__pfet_01v8[gds] @m.xm10.msky130_fd_pr__pfet_01v8[cgg] @m.xm10.msky130_fd_pr__pfet_01v8[cgs]
+ @m.xm10.msky130_fd_pr__pfet_01v8[cgd] @m.xm10.msky130_fd_pr__pfet_01v8[cgb] @m.xm10.msky130_fd_pr__pfet_01v8[cdg]
+ @m.xm10.msky130_fd_pr__pfet_01v8[cds] @m.xm10.msky130_fd_pr__pfet_01v8[cdd] @m.xm10.msky130_fd_pr__pfet_01v8[cdb]
+ @m.xm10.msky130_fd_pr__pfet_01v8[csg] @m.xm10.msky130_fd_pr__pfet_01v8[css] @m.xm10.msky130_fd_pr__pfet_01v8[csd]
+ @m.xm10.msky130_fd_pr__pfet_01v8[csb] @m.xm10.msky130_fd_pr__pfet_01v8[cbg] @m.xm10.msky130_fd_pr__pfet_01v8[cbs]
+ @m.xm10.msky130_fd_pr__pfet_01v8[cbd] @m.xm10.msky130_fd_pr__pfet_01v8[cbb]
save @m.xm13.msky130_fd_pr__pfet_01v8[vds] @m.xm13.msky130_fd_pr__pfet_01v8[gm]
+ @m.xm13.msky130_fd_pr__pfet_01v8[vth] @m.xm13.msky130_fd_pr__pfet_01v8[vgs] @m.xm13.msky130_fd_pr__pfet_01v8[id]
+ @m.xm13.msky130_fd_pr__pfet_01v8[gds] @m.xm13.msky130_fd_pr__pfet_01v8[cgg] @m.xm13.msky130_fd_pr__pfet_01v8[cgs]
+ @m.xm13.msky130_fd_pr__pfet_01v8[cgd] @m.xm13.msky130_fd_pr__pfet_01v8[cgb] @m.xm13.msky130_fd_pr__pfet_01v8[cdg]
+ @m.xm13.msky130_fd_pr__pfet_01v8[cds] @m.xm13.msky130_fd_pr__pfet_01v8[cdd] @m.xm13.msky130_fd_pr__pfet_01v8[cdb]
+ @m.xm13.msky130_fd_pr__pfet_01v8[csg] @m.xm13.msky130_fd_pr__pfet_01v8[css] @m.xm13.msky130_fd_pr__pfet_01v8[csd]
+ @m.xm13.msky130_fd_pr__pfet_01v8[csb] @m.xm13.msky130_fd_pr__pfet_01v8[cbg] @m.xm13.msky130_fd_pr__pfet_01v8[cbs]
+ @m.xm13.msky130_fd_pr__pfet_01v8[cbd] @m.xm13.msky130_fd_pr__pfet_01v8[cbb]
save @m.xm14.msky130_fd_pr__pfet_01v8[vds] @m.xm14.msky130_fd_pr__pfet_01v8[gm]
+ @m.xm14.msky130_fd_pr__pfet_01v8[vth] @m.xm14.msky130_fd_pr__pfet_01v8[vgs] @m.xm14.msky130_fd_pr__pfet_01v8[id]
+ @m.xm14.msky130_fd_pr__pfet_01v8[gds] @m.xm14.msky130_fd_pr__pfet_01v8[cgg] @m.xm14.msky130_fd_pr__pfet_01v8[cgs]
+ @m.xm14.msky130_fd_pr__pfet_01v8[cgd] @m.xm14.msky130_fd_pr__pfet_01v8[cgb] @m.xm14.msky130_fd_pr__pfet_01v8[cdg]
+ @m.xm14.msky130_fd_pr__pfet_01v8[cds] @m.xm14.msky130_fd_pr__pfet_01v8[cdd] @m.xm14.msky130_fd_pr__pfet_01v8[cdb]
+ @m.xm14.msky130_fd_pr__pfet_01v8[csg] @m.xm14.msky130_fd_pr__pfet_01v8[css] @m.xm14.msky130_fd_pr__pfet_01v8[csd]
+ @m.xm14.msky130_fd_pr__pfet_01v8[csb] @m.xm14.msky130_fd_pr__pfet_01v8[cbg] @m.xm14.msky130_fd_pr__pfet_01v8[cbs]
+ @m.xm14.msky130_fd_pr__pfet_01v8[cbd] @m.xm14.msky130_fd_pr__pfet_01v8[cbb]
save @m.xm24.msky130_fd_pr__pfet_01v8[vds] @m.xm24.msky130_fd_pr__pfet_01v8[gm]
+ @m.xm24.msky130_fd_pr__pfet_01v8[vth] @m.xm24.msky130_fd_pr__pfet_01v8[vgs] @m.xm24.msky130_fd_pr__pfet_01v8[id]
+ @m.xm24.msky130_fd_pr__pfet_01v8[gds] @m.xm24.msky130_fd_pr__pfet_01v8[cgg] @m.xm24.msky130_fd_pr__pfet_01v8[cgs]
+ @m.xm24.msky130_fd_pr__pfet_01v8[cgd] @m.xm24.msky130_fd_pr__pfet_01v8[cgb] @m.xm24.msky130_fd_pr__pfet_01v8[cdg]
+ @m.xm24.msky130_fd_pr__pfet_01v8[cds] @m.xm24.msky130_fd_pr__pfet_01v8[cdd] @m.xm24.msky130_fd_pr__pfet_01v8[cdb]
+ @m.xm24.msky130_fd_pr__pfet_01v8[csg] @m.xm24.msky130_fd_pr__pfet_01v8[css] @m.xm24.msky130_fd_pr__pfet_01v8[csd]
+ @m.xm24.msky130_fd_pr__pfet_01v8[csb] @m.xm24.msky130_fd_pr__pfet_01v8[cbg] @m.xm24.msky130_fd_pr__pfet_01v8[cbs]
+ @m.xm24.msky130_fd_pr__pfet_01v8[cbd] @m.xm24.msky130_fd_pr__pfet_01v8[cbb]
save @m.xm25.msky130_fd_pr__pfet_01v8[vds] @m.xm25.msky130_fd_pr__pfet_01v8[gm]
+ @m.xm25.msky130_fd_pr__pfet_01v8[vth] @m.xm25.msky130_fd_pr__pfet_01v8[vgs] @m.xm25.msky130_fd_pr__pfet_01v8[id]
+ @m.xm25.msky130_fd_pr__pfet_01v8[gds] @m.xm25.msky130_fd_pr__pfet_01v8[cgg] @m.xm25.msky130_fd_pr__pfet_01v8[cgs]
+ @m.xm25.msky130_fd_pr__pfet_01v8[cgd] @m.xm25.msky130_fd_pr__pfet_01v8[cgb] @m.xm25.msky130_fd_pr__pfet_01v8[cdg]
+ @m.xm25.msky130_fd_pr__pfet_01v8[cds] @m.xm25.msky130_fd_pr__pfet_01v8[cdd] @m.xm25.msky130_fd_pr__pfet_01v8[cdb]
+ @m.xm25.msky130_fd_pr__pfet_01v8[csg] @m.xm25.msky130_fd_pr__pfet_01v8[css] @m.xm25.msky130_fd_pr__pfet_01v8[csd]
+ @m.xm25.msky130_fd_pr__pfet_01v8[csb] @m.xm25.msky130_fd_pr__pfet_01v8[cbg] @m.xm25.msky130_fd_pr__pfet_01v8[cbs]
+ @m.xm25.msky130_fd_pr__pfet_01v8[cbd] @m.xm25.msky130_fd_pr__pfet_01v8[cbb]

op
write top_pex_tb.raw
.endc


.control
*set sqrnoise

*noise v(Vout_n) IINN_source dec 10 1 10000T
*noise v(Vout_n) IINN_source dec 50 1 100G
noise v(Vout_p) IINN_source dec 10 20k 1g
*setplot noise1
*plot loglog onoise_spectrum

setplot noise2
print onoise_total
*exit
.endc


**** end user architecture code
**.ends
.GLOBAL GND
.end
